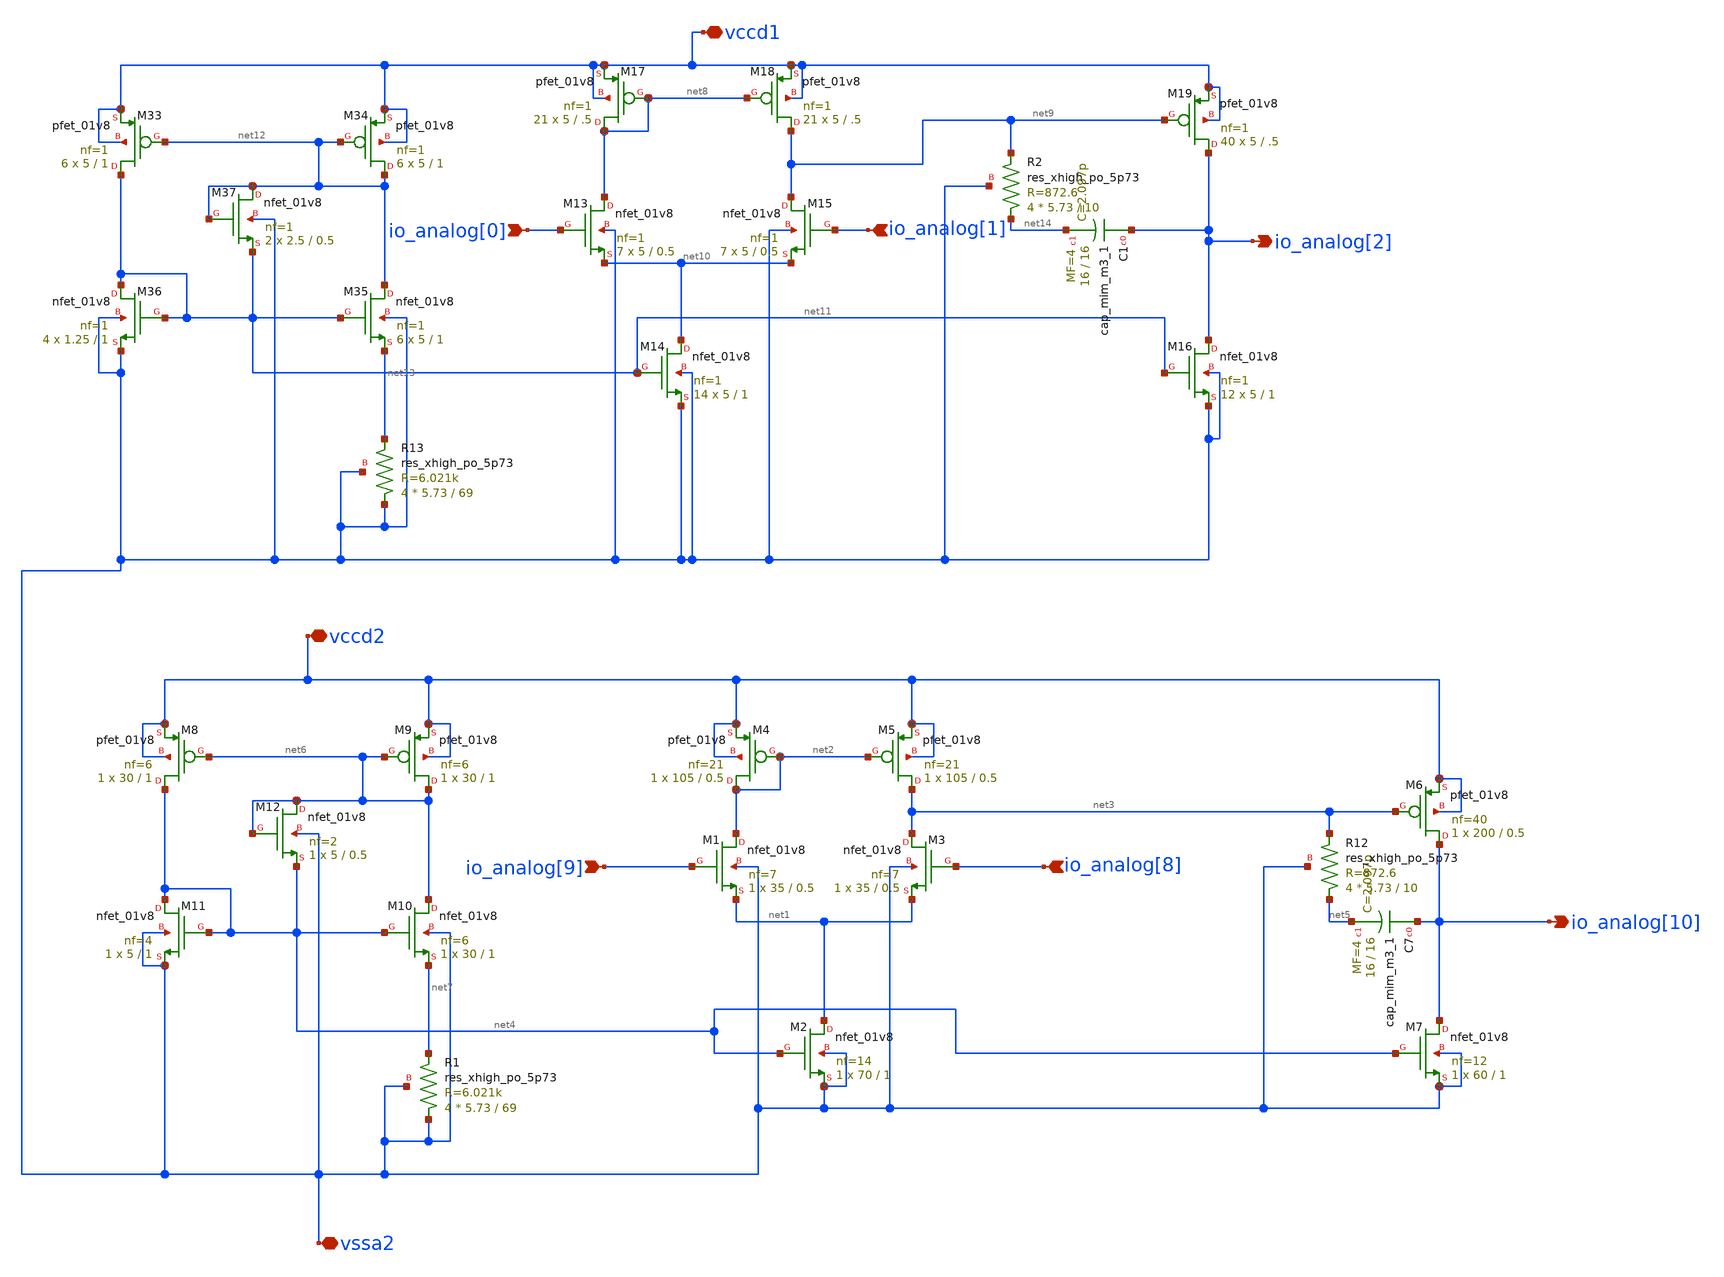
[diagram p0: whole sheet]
** sch_path: SP23_Tapeout/Tapeout_Ready_v5/OTA_GM_Schematic/user_analog_project_wrapper.sch
**.subckt user_analog_project_wrapper io_analog[2] io_analog[10] io_analog[9] io_analog[0]
*+ io_analog[1] vssa2 vccd2 vccd1 io_analog[8]
*.opin io_analog[2]
*.opin io_analog[10]
*.ipin io_analog[9]
*.ipin io_analog[0]
*.ipin io_analog[1]
*.iopin vssa2
*.iopin vccd2
*.iopin vccd1
*.ipin io_analog[8]
XM2 net1 net4 vssa2 vssa2 sky130_fd_pr__nfet_01v8 L=1 W=70 nf=14 ad='int((nf+1)/2) * W/nf * 0.29' as='int((nf+2)/2) * W/nf * 0.29'
+ pd='2*int((nf+1)/2) * (W/nf + 0.29)' ps='2*int((nf+2)/2) * (W/nf + 0.29)' nrd='0.29 / W' nrs='0.29 / W'
+ sa=0 sb=0 sd=0 mult=1 m=1
XM1 net2 io_analog[9] net1 vssa2 sky130_fd_pr__nfet_01v8 L=0.5 W=35 nf=7 ad='int((nf+1)/2) * W/nf * 0.29'
+ as='int((nf+2)/2) * W/nf * 0.29' pd='2*int((nf+1)/2) * (W/nf + 0.29)' ps='2*int((nf+2)/2) * (W/nf + 0.29)'
+ nrd='0.29 / W' nrs='0.29 / W' sa=0 sb=0 sd=0 mult=1 m=1
XM3 net3 io_analog[8] net1 vssa2 sky130_fd_pr__nfet_01v8 L=0.5 W=35 nf=7 ad='int((nf+1)/2) * W/nf * 0.29'
+ as='int((nf+2)/2) * W/nf * 0.29' pd='2*int((nf+1)/2) * (W/nf + 0.29)' ps='2*int((nf+2)/2) * (W/nf + 0.29)'
+ nrd='0.29 / W' nrs='0.29 / W' sa=0 sb=0 sd=0 mult=1 m=1
XM4 net2 net2 vccd2 vccd2 sky130_fd_pr__pfet_01v8 L=0.5 W=105 nf=21 ad='int((nf+1)/2) * W/nf * 0.29'
+ as='int((nf+2)/2) * W/nf * 0.29' pd='2*int((nf+1)/2) * (W/nf + 0.29)' ps='2*int((nf+2)/2) * (W/nf + 0.29)'
+ nrd='0.29 / W' nrs='0.29 / W' sa=0 sb=0 sd=0 mult=1 m=1
XM5 net3 net2 vccd2 vccd2 sky130_fd_pr__pfet_01v8 L=0.5 W=105 nf=21 ad='int((nf+1)/2) * W/nf * 0.29'
+ as='int((nf+2)/2) * W/nf * 0.29' pd='2*int((nf+1)/2) * (W/nf + 0.29)' ps='2*int((nf+2)/2) * (W/nf + 0.29)'
+ nrd='0.29 / W' nrs='0.29 / W' sa=0 sb=0 sd=0 mult=1 m=1
XM6 io_analog[10] net3 vccd2 vccd2 sky130_fd_pr__pfet_01v8 L=0.5 W=200 nf=40 ad='int((nf+1)/2) * W/nf * 0.29'
+ as='int((nf+2)/2) * W/nf * 0.29' pd='2*int((nf+1)/2) * (W/nf + 0.29)' ps='2*int((nf+2)/2) * (W/nf + 0.29)'
+ nrd='0.29 / W' nrs='0.29 / W' sa=0 sb=0 sd=0 mult=1 m=1
XM7 io_analog[10] net4 vssa2 vssa2 sky130_fd_pr__nfet_01v8 L=1 W=60 nf=12 ad='int((nf+1)/2) * W/nf * 0.29'
+ as='int((nf+2)/2) * W/nf * 0.29' pd='2*int((nf+1)/2) * (W/nf + 0.29)' ps='2*int((nf+2)/2) * (W/nf + 0.29)'
+ nrd='0.29 / W' nrs='0.29 / W' sa=0 sb=0 sd=0 mult=1 m=1
XC7 io_analog[10] net5 sky130_fd_pr__cap_mim_m3_1 W=16 L=16 MF=4 m=4
XR12 net5 net3 vssa2 sky130_fd_pr__res_xhigh_po_5p73 L=10 mult=4 m=4
XM8 net4 net6 vccd2 vccd2 sky130_fd_pr__pfet_01v8 L=1 W=30 nf=6 ad='int((nf+1)/2) * W/nf * 0.29' as='int((nf+2)/2) * W/nf * 0.29'
+ pd='2*int((nf+1)/2) * (W/nf + 0.29)' ps='2*int((nf+2)/2) * (W/nf + 0.29)' nrd='0.29 / W' nrs='0.29 / W'
+ sa=0 sb=0 sd=0 mult=1 m=1
XM9 net6 net6 vccd2 vccd2 sky130_fd_pr__pfet_01v8 L=1 W=30 nf=6 ad='int((nf+1)/2) * W/nf * 0.29' as='int((nf+2)/2) * W/nf * 0.29'
+ pd='2*int((nf+1)/2) * (W/nf + 0.29)' ps='2*int((nf+2)/2) * (W/nf + 0.29)' nrd='0.29 / W' nrs='0.29 / W'
+ sa=0 sb=0 sd=0 mult=1 m=1
XM10 net6 net4 net7 vssa2 sky130_fd_pr__nfet_01v8 L=1 W=30 nf=6 ad='int((nf+1)/2) * W/nf * 0.29' as='int((nf+2)/2) * W/nf * 0.29'
+ pd='2*int((nf+1)/2) * (W/nf + 0.29)' ps='2*int((nf+2)/2) * (W/nf + 0.29)' nrd='0.29 / W' nrs='0.29 / W'
+ sa=0 sb=0 sd=0 mult=1 m=1
XM11 net4 net4 vssa2 vssa2 sky130_fd_pr__nfet_01v8 L=1 W=5 nf=4 ad='int((nf+1)/2) * W/nf * 0.29' as='int((nf+2)/2) * W/nf * 0.29'
+ pd='2*int((nf+1)/2) * (W/nf + 0.29)' ps='2*int((nf+2)/2) * (W/nf + 0.29)' nrd='0.29 / W' nrs='0.29 / W'
+ sa=0 sb=0 sd=0 mult=1 m=1
XM12 net6 net6 net4 vssa2 sky130_fd_pr__nfet_01v8 L=0.5 W=5 nf=2 ad='int((nf+1)/2) * W/nf * 0.29' as='int((nf+2)/2) * W/nf * 0.29'
+ pd='2*int((nf+1)/2) * (W/nf + 0.29)' ps='2*int((nf+2)/2) * (W/nf + 0.29)' nrd='0.29 / W' nrs='0.29 / W'
+ sa=0 sb=0 sd=0 mult=1 m=1
XR1 vssa2 net7 vssa2 sky130_fd_pr__res_xhigh_po_5p73 L=69 mult=4 m=4
XM13 net8 io_analog[0] net10 vssa2 sky130_fd_pr__nfet_01v8 L=0.5 W=5 nf=1 ad='int((nf+1)/2) * W/nf * 0.29'
+ as='int((nf+2)/2) * W/nf * 0.29' pd='2*int((nf+1)/2) * (W/nf + 0.29)' ps='2*int((nf+2)/2) * (W/nf + 0.29)'
+ nrd='0.29 / W' nrs='0.29 / W' sa=0 sb=0 sd=0 mult=7 m=7
XM14 net10 net11 vssa2 vssa2 sky130_fd_pr__nfet_01v8 L=1 W=5 nf=1 ad='int((nf+1)/2) * W/nf * 0.29' as='int((nf+2)/2) * W/nf * 0.29'
+ pd='2*int((nf+1)/2) * (W/nf + 0.29)' ps='2*int((nf+2)/2) * (W/nf + 0.29)' nrd='0.29 / W' nrs='0.29 / W'
+ sa=0 sb=0 sd=0 mult=14 m=14
XM15 net9 io_analog[1] net10 vssa2 sky130_fd_pr__nfet_01v8 L=0.5 W=5 nf=1 ad='int((nf+1)/2) * W/nf * 0.29'
+ as='int((nf+2)/2) * W/nf * 0.29' pd='2*int((nf+1)/2) * (W/nf + 0.29)' ps='2*int((nf+2)/2) * (W/nf + 0.29)'
+ nrd='0.29 / W' nrs='0.29 / W' sa=0 sb=0 sd=0 mult=7 m=7
XM16 io_analog[2] net11 vssa2 vssa2 sky130_fd_pr__nfet_01v8 L=1 W=5 nf=1 ad='int((nf+1)/2) * W/nf * 0.29'
+ as='int((nf+2)/2) * W/nf * 0.29' pd='2*int((nf+1)/2) * (W/nf + 0.29)' ps='2*int((nf+2)/2) * (W/nf + 0.29)'
+ nrd='0.29 / W' nrs='0.29 / W' sa=0 sb=0 sd=0 mult=12 m=12
XM17 net8 net8 vccd1 vccd1 sky130_fd_pr__pfet_01v8 L=.5 W=5 nf=1 ad='int((nf+1)/2) * W/nf * 0.29' as='int((nf+2)/2) * W/nf * 0.29'
+ pd='2*int((nf+1)/2) * (W/nf + 0.29)' ps='2*int((nf+2)/2) * (W/nf + 0.29)' nrd='0.29 / W' nrs='0.29 / W'
+ sa=0 sb=0 sd=0 mult=21 m=21
XM18 net9 net8 vccd1 vccd1 sky130_fd_pr__pfet_01v8 L=.5 W=5 nf=1 ad='int((nf+1)/2) * W/nf * 0.29' as='int((nf+2)/2) * W/nf * 0.29'
+ pd='2*int((nf+1)/2) * (W/nf + 0.29)' ps='2*int((nf+2)/2) * (W/nf + 0.29)' nrd='0.29 / W' nrs='0.29 / W'
+ sa=0 sb=0 sd=0 mult=21 m=21
XM19 io_analog[2] net9 vccd1 vccd1 sky130_fd_pr__pfet_01v8 L=.5 W=5 nf=1 ad='int((nf+1)/2) * W/nf * 0.29'
+ as='int((nf+2)/2) * W/nf * 0.29' pd='2*int((nf+1)/2) * (W/nf + 0.29)' ps='2*int((nf+2)/2) * (W/nf + 0.29)'
+ nrd='0.29 / W' nrs='0.29 / W' sa=0 sb=0 sd=0 mult=40 m=40
XR2 net14 net9 vssa2 sky130_fd_pr__res_xhigh_po_5p73 L=10 mult=4 m=4
XC1 io_analog[2] net14 sky130_fd_pr__cap_mim_m3_1 W=16 L=16 MF=4 m=4
XM33 net11 net12 vccd1 vccd1 sky130_fd_pr__pfet_01v8 L=1 W=5 nf=1 ad='int((nf+1)/2) * W/nf * 0.29' as='int((nf+2)/2) * W/nf * 0.29'
+ pd='2*int((nf+1)/2) * (W/nf + 0.29)' ps='2*int((nf+2)/2) * (W/nf + 0.29)' nrd='0.29 / W' nrs='0.29 / W'
+ sa=0 sb=0 sd=0 mult=6 m=6
XM34 net12 net12 vccd1 vccd1 sky130_fd_pr__pfet_01v8 L=1 W=5 nf=1 ad='int((nf+1)/2) * W/nf * 0.29' as='int((nf+2)/2) * W/nf * 0.29'
+ pd='2*int((nf+1)/2) * (W/nf + 0.29)' ps='2*int((nf+2)/2) * (W/nf + 0.29)' nrd='0.29 / W' nrs='0.29 / W'
+ sa=0 sb=0 sd=0 mult=6 m=6
XM35 net12 net11 net13 vssa2 sky130_fd_pr__nfet_01v8 L=1 W=5 nf=1 ad='int((nf+1)/2) * W/nf * 0.29' as='int((nf+2)/2) * W/nf * 0.29'
+ pd='2*int((nf+1)/2) * (W/nf + 0.29)' ps='2*int((nf+2)/2) * (W/nf + 0.29)' nrd='0.29 / W' nrs='0.29 / W'
+ sa=0 sb=0 sd=0 mult=6 m=6
XM36 net11 net11 vssa2 vssa2 sky130_fd_pr__nfet_01v8 L=1 W=1.25 nf=1 ad='int((nf+1)/2) * W/nf * 0.29'
+ as='int((nf+2)/2) * W/nf * 0.29' pd='2*int((nf+1)/2) * (W/nf + 0.29)' ps='2*int((nf+2)/2) * (W/nf + 0.29)'
+ nrd='0.29 / W' nrs='0.29 / W' sa=0 sb=0 sd=0 mult=4 m=4
XM37 net12 net12 net11 vssa2 sky130_fd_pr__nfet_01v8 L=0.5 W=2.5 nf=1 ad='int((nf+1)/2) * W/nf * 0.29'
+ as='int((nf+2)/2) * W/nf * 0.29' pd='2*int((nf+1)/2) * (W/nf + 0.29)' ps='2*int((nf+2)/2) * (W/nf + 0.29)'
+ nrd='0.29 / W' nrs='0.29 / W' sa=0 sb=0 sd=0 mult=2 m=2
XR13 vssa2 net13 vssa2 sky130_fd_pr__res_xhigh_po_5p73 L=69 mult=4 m=4
**.ends
.end
